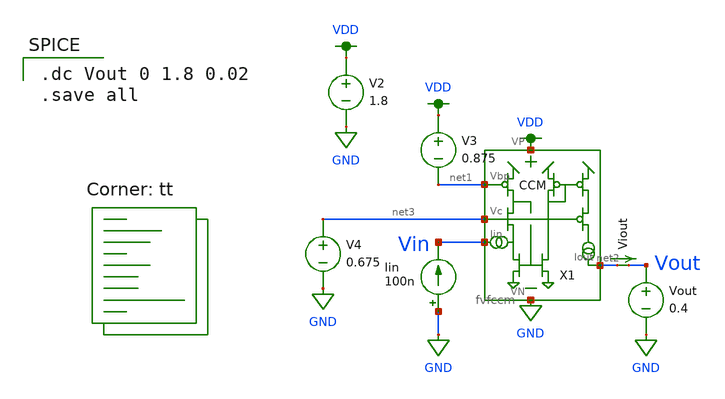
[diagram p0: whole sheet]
** sch_path: test_fvfccm_2.sch
**.subckt test_fvfccm_2
Iin GND Vin 100n
V2 VDD GND 1.8
X1 VDD net1 Vin GND net2 net3 fvfccm
V3 VDD net1 0.875
Vout Vout GND 0.4
Viout net2 Vout 0
.save i(viout)
V4 net3 GND 0.675
**** begin user architecture code

.dc Vout 0 1.8 0.02
.save all

.lib $::SKYWATER_MODELS/sky130.lib.spice tt
**** end user architecture code
**.ends
.GLOBAL GND
.GLOBAL VDD
.end
